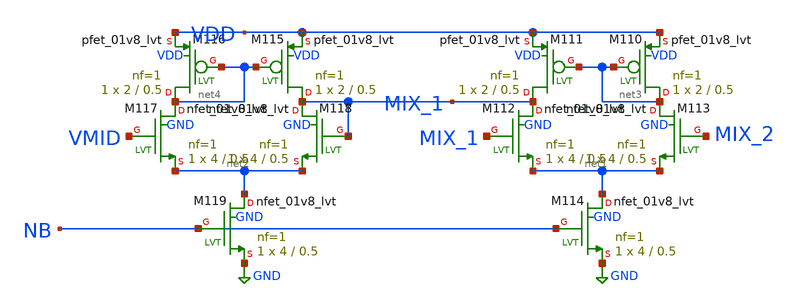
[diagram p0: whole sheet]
** sch_path: xschem/xschemwrap/analogsub.sch
**.subckt analogsub
XM110 net3 net3 VDD VDD sky130_fd_pr__pfet_01v8_lvt L=0.5 W=2 nf=1 ad='int((1 + 1)/2) * 2 / 1 * 0.29'
+ as='int((1 + 2)/2) * 2 / 1 * 0.29' pd='2*int((1 + 1)/2) * (2 / 1 + 0.29)' ps='2*int((1 + 2)/2) * (2 / 1 + 0.29)'
+ nrd='0.29 / 2 ' nrs='0.29 / 2 ' sa=0 sb=0 sd=0 mult=1 m=1
XM111 MIX_1 net3 VDD VDD sky130_fd_pr__pfet_01v8_lvt L=0.5 W=2 nf=1 ad='int((1 + 1)/2) * 2 / 1 * 0.29'
+ as='int((1 + 2)/2) * 2 / 1 * 0.29' pd='2*int((1 + 1)/2) * (2 / 1 + 0.29)' ps='2*int((1 + 2)/2) * (2 / 1 + 0.29)'
+ nrd='0.29 / 2 ' nrs='0.29 / 2 ' sa=0 sb=0 sd=0 mult=1 m=1
XM112 MIX_1 MIX_1 net1 GND sky130_fd_pr__nfet_01v8_lvt L=0.5 W=4 nf=1 ad='int((1 + 1)/2) * 4 / 1 * 0.29'
+ as='int((1 + 2)/2) * 4 / 1 * 0.29' pd='2*int((1 + 1)/2) * (4 / 1 + 0.29)' ps='2*int((1 + 2)/2) * (4 / 1 + 0.29)'
+ nrd='0.29 / 4 ' nrs='0.29 / 4 ' sa=0 sb=0 sd=0 mult=1 m=1
XM113 net3 MIX_2 net1 GND sky130_fd_pr__nfet_01v8_lvt L=0.5 W=4 nf=1 ad='int((1 + 1)/2) * 4 / 1 * 0.29'
+ as='int((1 + 2)/2) * 4 / 1 * 0.29' pd='2*int((1 + 1)/2) * (4 / 1 + 0.29)' ps='2*int((1 + 2)/2) * (4 / 1 + 0.29)'
+ nrd='0.29 / 4 ' nrs='0.29 / 4 ' sa=0 sb=0 sd=0 mult=1 m=1
XM114 net1 NB GND GND sky130_fd_pr__nfet_01v8_lvt L=0.5 W=4 nf=1 ad='int((1 + 1)/2) * 4 / 1 * 0.29' as='int((1 + 2)/2) * 4 / 1 * 0.29'
+ pd='2*int((1 + 1)/2) * (4 / 1 + 0.29)' ps='2*int((1 + 2)/2) * (4 / 1 + 0.29)' nrd='0.29 / 4 ' nrs='0.29 / 4 '
+ sa=0 sb=0 sd=0 mult=1 m=1
XM115 MIX_1 net4 VDD VDD sky130_fd_pr__pfet_01v8_lvt L=0.5 W=2 nf=1 ad='int((1 + 1)/2) * 2 / 1 * 0.29'
+ as='int((1 + 2)/2) * 2 / 1 * 0.29' pd='2*int((1 + 1)/2) * (2 / 1 + 0.29)' ps='2*int((1 + 2)/2) * (2 / 1 + 0.29)'
+ nrd='0.29 / 2 ' nrs='0.29 / 2 ' sa=0 sb=0 sd=0 mult=1 m=1
XM116 net4 net4 VDD VDD sky130_fd_pr__pfet_01v8_lvt L=0.5 W=2 nf=1 ad='int((1 + 1)/2) * 2 / 1 * 0.29'
+ as='int((1 + 2)/2) * 2 / 1 * 0.29' pd='2*int((1 + 1)/2) * (2 / 1 + 0.29)' ps='2*int((1 + 2)/2) * (2 / 1 + 0.29)'
+ nrd='0.29 / 2 ' nrs='0.29 / 2 ' sa=0 sb=0 sd=0 mult=1 m=1
XM117 net4 VMID net2 GND sky130_fd_pr__nfet_01v8_lvt L=0.5 W=4 nf=1 ad='int((1 + 1)/2) * 4 / 1 * 0.29'
+ as='int((1 + 2)/2) * 4 / 1 * 0.29' pd='2*int((1 + 1)/2) * (4 / 1 + 0.29)' ps='2*int((1 + 2)/2) * (4 / 1 + 0.29)'
+ nrd='0.29 / 4 ' nrs='0.29 / 4 ' sa=0 sb=0 sd=0 mult=1 m=1
XM118 MIX_1 MIX_1 net2 GND sky130_fd_pr__nfet_01v8_lvt L=0.5 W=4 nf=1 ad='int((1 + 1)/2) * 4 / 1 * 0.29'
+ as='int((1 + 2)/2) * 4 / 1 * 0.29' pd='2*int((1 + 1)/2) * (4 / 1 + 0.29)' ps='2*int((1 + 2)/2) * (4 / 1 + 0.29)'
+ nrd='0.29 / 4 ' nrs='0.29 / 4 ' sa=0 sb=0 sd=0 mult=1 m=1
XM119 net2 NB GND GND sky130_fd_pr__nfet_01v8_lvt L=0.5 W=4 nf=1 ad='int((1 + 1)/2) * 4 / 1 * 0.29' as='int((1 + 2)/2) * 4 / 1 * 0.29'
+ pd='2*int((1 + 1)/2) * (4 / 1 + 0.29)' ps='2*int((1 + 2)/2) * (4 / 1 + 0.29)' nrd='0.29 / 4 ' nrs='0.29 / 4 '
+ sa=0 sb=0 sd=0 mult=1 m=1
**.ends
.GLOBAL GND
.end
